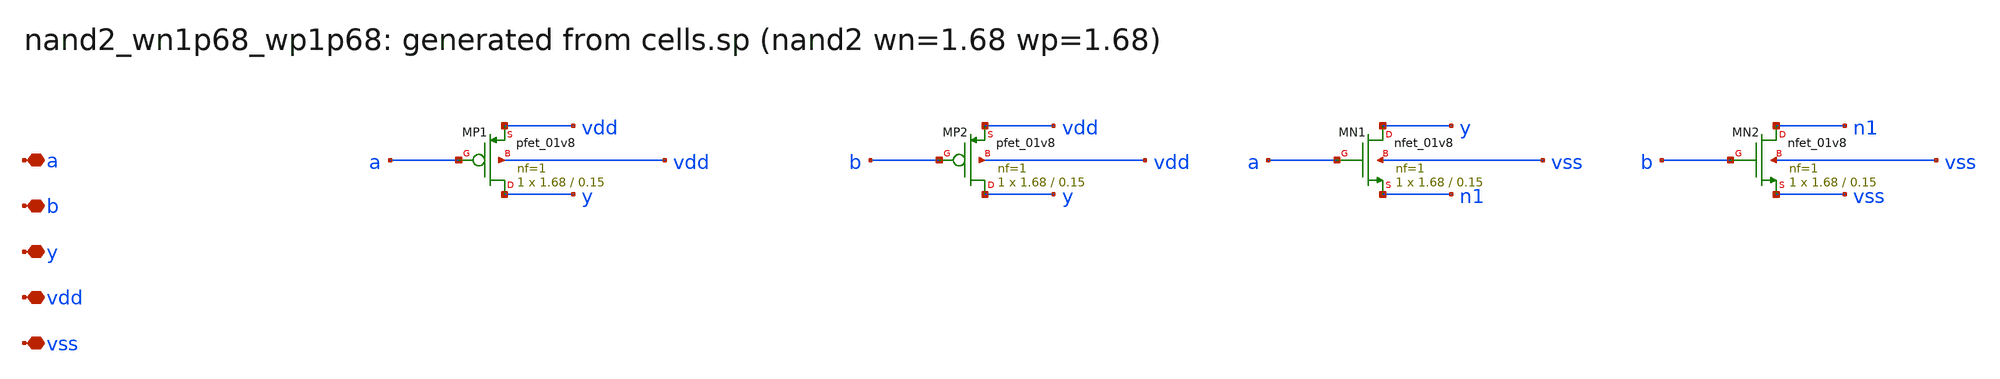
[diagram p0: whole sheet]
** sch_path: sram/xschem/nand2_wn1p68_wp1p68.sch
**.subckt nand2_wn1p68_wp1p68 a b y vdd vss
*.iopin a
*.iopin b
*.iopin y
*.iopin vdd
*.iopin vss
XMP1 y a vdd vdd sky130_fd_pr__pfet_01v8 L=0.15 W=1.68 nf=1 ad='int((nf+1)/2) * W/nf * 0.29' as='int((nf+2)/2) * W/nf * 0.29'
+ pd='2*int((nf+1)/2) * (W/nf + 0.29)' ps='2*int((nf+2)/2) * (W/nf + 0.29)' nrd='0.29 / W' nrs='0.29 / W'
+ sa=0 sb=0 sd=0 mult=1 m=1
XMP2 y b vdd vdd sky130_fd_pr__pfet_01v8 L=0.15 W=1.68 nf=1 ad='int((nf+1)/2) * W/nf * 0.29' as='int((nf+2)/2) * W/nf * 0.29'
+ pd='2*int((nf+1)/2) * (W/nf + 0.29)' ps='2*int((nf+2)/2) * (W/nf + 0.29)' nrd='0.29 / W' nrs='0.29 / W'
+ sa=0 sb=0 sd=0 mult=1 m=1
XMN1 y a n1 vss sky130_fd_pr__nfet_01v8 L=0.15 W=1.68 nf=1 ad='int((1 + 1)/2) * 1.68 / 1 * 0.29' as='int((1 + 2)/2) * 1.68 / 1 * 0.29'
+ pd='2*int((1 + 1)/2) * (1.68 / 1 + 0.29)' ps='2*int((1 + 2)/2) * (1.68 / 1 + 0.29)' nrd='0.29 / 1.68 '
+ nrs='0.29 / 1.68 ' sa=0 sb=0 sd=0 mult=1 m=1
XMN2 n1 b vss vss sky130_fd_pr__nfet_01v8 L=0.15 W=1.68 nf=1 ad='int((1 + 1)/2) * 1.68 / 1 * 0.29' as='int((1 + 2)/2) * 1.68 / 1 * 0.29'
+ pd='2*int((1 + 1)/2) * (1.68 / 1 + 0.29)' ps='2*int((1 + 2)/2) * (1.68 / 1 + 0.29)' nrd='0.29 / 1.68 '
+ nrs='0.29 / 1.68 ' sa=0 sb=0 sd=0 mult=1 m=1
**.ends
.end
